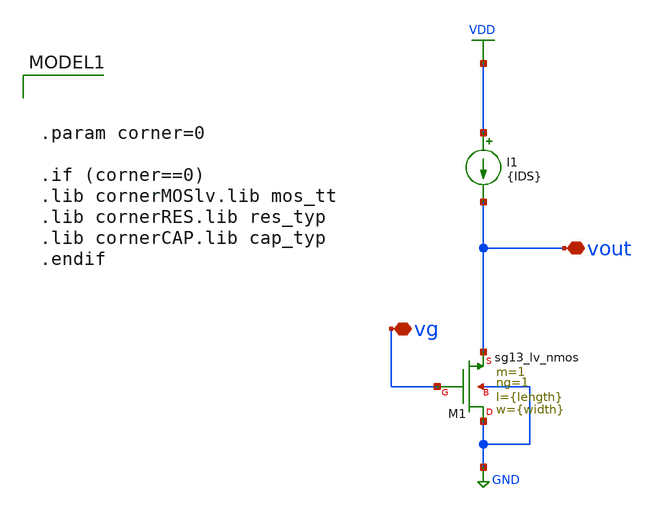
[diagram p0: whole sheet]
** sch_path: Tarea1/xschem/cs_amp_full.sch
**.subckt cs_amp_full vg vout
*.iopin vg
*.iopin vout
I1 VDD vout {IDS}
XM1 GND vg vout GND sg13_lv_nmos w={width} l={length} ng=1 m=1 mm_ok=1
**** begin user architecture code


.param corner=0

.if (corner==0)
.lib cornerMOSlv.lib mos_tt
.lib cornerRES.lib res_typ
.lib cornerCAP.lib cap_typ
.endif



.option wnflag=1
.param IDS = {120u*3.141596}
.param length = 0.5u
.param width = 0.4u

vsup VDD 0 1.8
vin vg 0 dc={0.35} ac=1

cload vout 0 5p

.control
save all
op
save @n.xm1.nsg13_lv_nmos[gm]
save @n.xm1.nsg13_lv_nmos[ids]
save @n.xm1.nsg13_lv_nmos[gds]
save @n.xm1.nsg13_lv_nmos[ib]

*dc vin -0.01 0.01 0.001
dc vin 0.35 0.35 0.001

let gdsn = @n.xm1.nsg13_lv_nmos[gds]
let gmn = @n.xm1.nsg13_lv_nmos[gm]
let vthn = @n.xm1.nsg13_lv_nmos[vth]
let idn = @n.xm1.nsg13_lv_nmos[ids]
let ao = gmn / gdsn

print vthn
print ao

ac dec 100 1 1T
*plot vdb(vout)
meas ac GBW when vdb(vout)=0
meas ac DCG find vdb(vout) at=1]]
op
*print vout
*print vg
.endc

**** end user architecture code
**.ends
.GLOBAL GND
.GLOBAL VDD
.end
